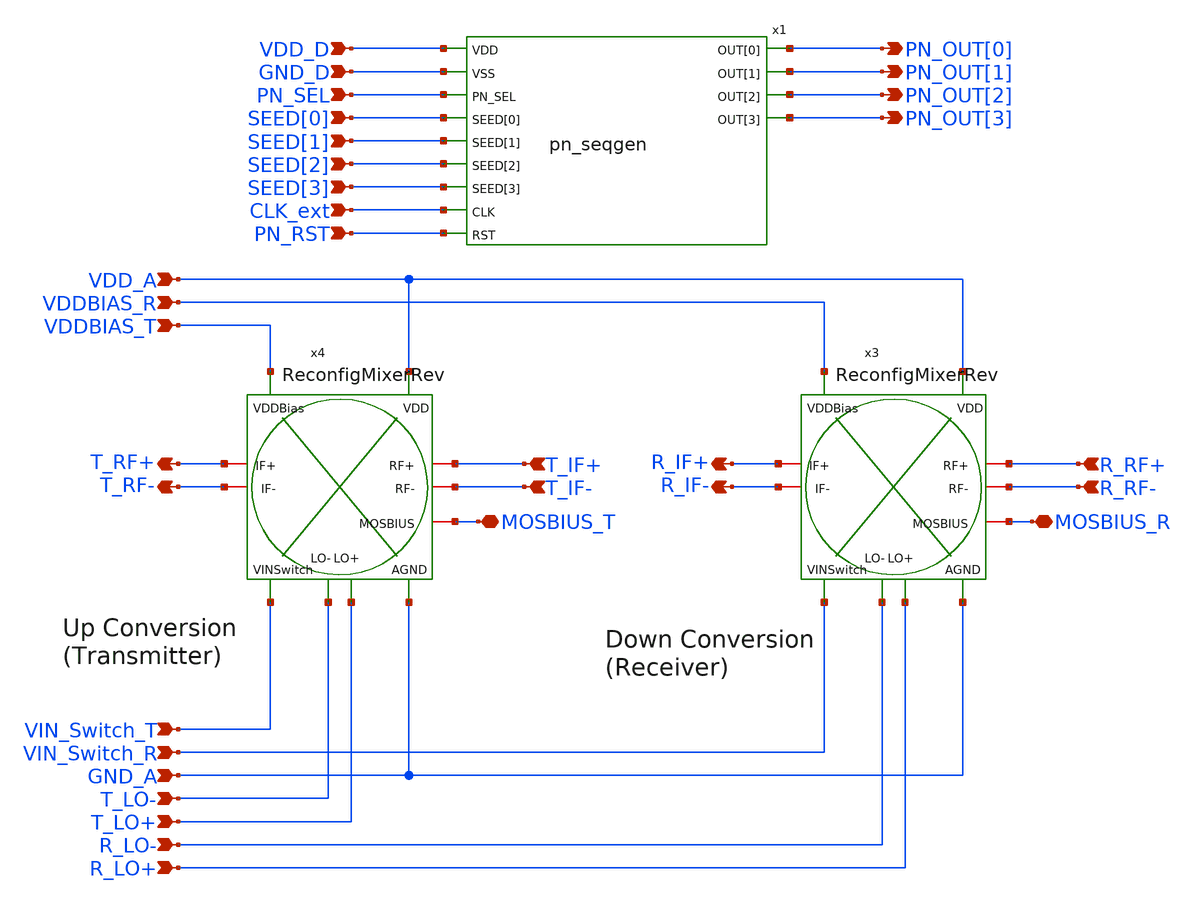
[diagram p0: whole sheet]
** sch_path: Project/1-on-chip/schematic/TOPLEVEL.sch
**.subckt TOPLEVEL T_RF+ T_RF- R_IF+ R_IF- VDD_D GND_D PN_SEL SEED[0] SEED[1] SEED[2] SEED[3]
*+ CLK_ext PN_RST PN_OUT[0] PN_OUT[1] PN_OUT[2] PN_OUT[3] VDDBIAS_T VDDBIAS_R VDD_A MOSBIUS_T MOSBIUS_R T_IF+
*+ T_IF- R_RF+ R_RF- GND_A VIN_Switch_R VIN_Switch_T T_LO+ T_LO- R_LO+ R_LO-
*.opin T_RF+
*.opin T_RF-
*.opin R_IF+
*.opin R_IF-
*.ipin VDD_D
*.ipin GND_D
*.ipin PN_SEL
*.ipin SEED[0]
*.ipin SEED[1]
*.ipin SEED[2]
*.ipin SEED[3]
*.ipin CLK_ext
*.ipin PN_RST
*.opin PN_OUT[0]
*.opin PN_OUT[1]
*.opin PN_OUT[2]
*.opin PN_OUT[3]
*.ipin VDDBIAS_T
*.ipin VDDBIAS_R
*.ipin VDD_A
*.iopin MOSBIUS_T
*.iopin MOSBIUS_R
*.ipin T_IF+
*.ipin T_IF-
*.ipin R_RF+
*.ipin R_RF-
*.ipin GND_A
*.ipin VIN_Switch_R
*.ipin VIN_Switch_T
*.ipin T_LO+
*.ipin T_LO-
*.ipin R_LO+
*.ipin R_LO-
x3 VDD_A R_IF+ R_IF- R_LO+ R_LO- R_RF+ R_RF- MOSBIUS_R VDDBIAS_R GND_A VIN_Switch_R ReconfigMixerRev
x4 VDD_A T_RF+ T_RF- T_LO+ T_LO- T_IF+ T_IF- MOSBIUS_T VDDBIAS_T GND_A VIN_Switch_T ReconfigMixerRev
x1 VDD_D GND_D PN_SEL SEED[0] SEED[1] SEED[2] SEED[3] CLK_ext PN_RST PN_OUT[0] PN_OUT[1] PN_OUT[2]
+ PN_OUT[3] pn_seqgen
**.ends
.end
